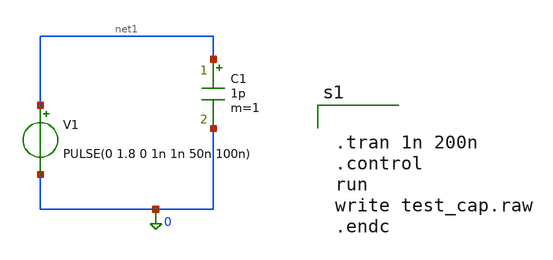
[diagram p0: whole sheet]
** sch_path: sch/test_cap.sch
**.subckt test_cap
C1 net1 0 1p m=1
V1 net1 0 PULSE(0 1.8 0 1n 1n 50n 100n)
**** begin user architecture code


.tran 1n 200n
.control
run
write test_cap.raw
.endc


**** end user architecture code
**.ends
.end
